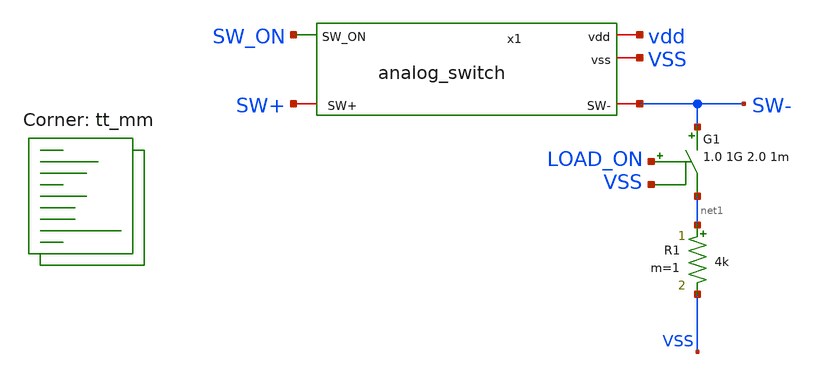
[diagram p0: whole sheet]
** sch_path: xschem/analog_switch_tb.sch
**.subckt analog_switch_tb
x1 vdd VSS SW_ON SW+ SW- analog_switch
R1 net1 VSS 4k m=1
G1 SW- net1 vcr pwl(1) LOAD_ON VSS 1.0 1G 2.0 1m
**** begin user architecture code
.lib $::SKYWATER_MODELS/sky130.lib.spice tt_mm

*.option method = gear
*.option wnflag = 1
.param VCC = agauss(1.8,0.5,1)
.option temp = aguass(40,30,1)
.include stimuli_tb_analog_switch.cir
.control
	option seed = 69
	let run = 0
	dowhile run <= 100
		save all
		tran 1n 8u uic
		remzerovec
		write tb_analog_switch.raw
		set appendwrite
		reset
		let run = run +1
	end
.endc



**** end user architecture code
**.ends

* expanding   symbol:  analog_switch.sym # of pins=5
** sym_path: xschem/analog_switch.sym
** sch_path: xschem/analog_switch.sch
.subckt analog_switch vdd vss SW_ON SW+ SW-
*.iopin vdd
*.iopin vss
*.ipin SW_ON
*.iopin SW+
*.iopin SW-
XM5 ~SW_ON SW_ON vss vss sky130_fd_pr__nfet_g5v0d10v5 L=0.5 W=1 nf=1 ad='int((1 + 1)/2) * 1 / 1 * 0.29'
+ as='int((1 + 2)/2) * 1 / 1 * 0.29' pd='2*int((1 + 1)/2) * (1 / 1 + 0.29)' ps='2*int((1 + 2)/2) * (1 / 1 + 0.29)'
+ nrd='0.29 / 1 ' nrs='0.29 / 1 ' sa=0 sb=0 sd=0 mult=1 m=1
XM9 ~SW_ON SW_ON vdd vdd sky130_fd_pr__pfet_g5v0d10v5 L=0.5 W=1 nf=1 ad='int((1 + 1)/2) * 1 / 1 * 0.29'
+ as='int((1 + 2)/2) * 1 / 1 * 0.29' pd='2*int((1 + 1)/2) * (1 / 1 + 0.29)' ps='2*int((1 + 2)/2) * (1 / 1 + 0.29)'
+ nrd='0.29 / 1 ' nrs='0.29 / 1 ' sa=0 sb=0 sd=0 mult=1 m=1
XM1 SW- SW_ON SW+ SW+ sky130_fd_pr__nfet_g5v0d10v5 L=15 W=w_swfet nf=1 ad='int((1 + 1)/2) * w_swfet / 1 * 0.29'
+ as='int((1 + 2)/2) * w_swfet / 1 * 0.29' pd='2*int((1 + 1)/2) * (w_swfet / 1 + 0.29)' ps='2*int((1 + 2)/2) * (w_swfet / 1 + 0.29)'
+ nrd='0.29 / w_swfet ' nrs='0.29 / w_swfet ' sa=0 sb=0 sd=0 mult=1 m=1
XM3 SW+ ~SW_ON SW- SW- sky130_fd_pr__pfet_g5v0d10v5 L=15 W=w_swfet nf=1 ad='int((1 + 1)/2) * w_swfet / 1 * 0.29'
+ as='int((1 + 2)/2) * w_swfet / 1 * 0.29' pd='2*int((1 + 1)/2) * (w_swfet / 1 + 0.29)' ps='2*int((1 + 2)/2) * (w_swfet / 1 + 0.29)'
+ nrd='0.29 / w_swfet ' nrs='0.29 / w_swfet ' sa=0 sb=0 sd=0 mult=1 m=1
XM2 SW- ~SW_ON SW- SW- sky130_fd_pr__nfet_g5v0d10v5 L=15 W=w_swfet/2 nf=1 ad='int((1 + 1)/2) * w_swfet/2 / 1 * 0.29'
+ as='int((1 + 2)/2) * w_swfet/2 / 1 * 0.29' pd='2*int((1 + 1)/2) * (w_swfet/2 / 1 + 0.29)' ps='2*int((1 + 2)/2) * (w_swfet/2 / 1 + 0.29)'
+ nrd='0.29 / w_swfet/2 ' nrs='0.29 / w_swfet/2 ' sa=0 sb=0 sd=0 mult=1 m=1
XM4 SW- SW_ON SW- SW- sky130_fd_pr__pfet_g5v0d10v5 L=15 W=w_swfet/2 nf=1 ad='int((1 + 1)/2) * w_swfet/2 / 1 * 0.29'
+ as='int((1 + 2)/2) * w_swfet/2 / 1 * 0.29' pd='2*int((1 + 1)/2) * (w_swfet/2 / 1 + 0.29)' ps='2*int((1 + 2)/2) * (w_swfet/2 / 1 + 0.29)'
+ nrd='0.29 / w_swfet/2 ' nrs='0.29 / w_swfet/2 ' sa=0 sb=0 sd=0 mult=1 m=1
**** begin user architecture code
w_swfets=16
**** end user architecture code
.ends

.end
